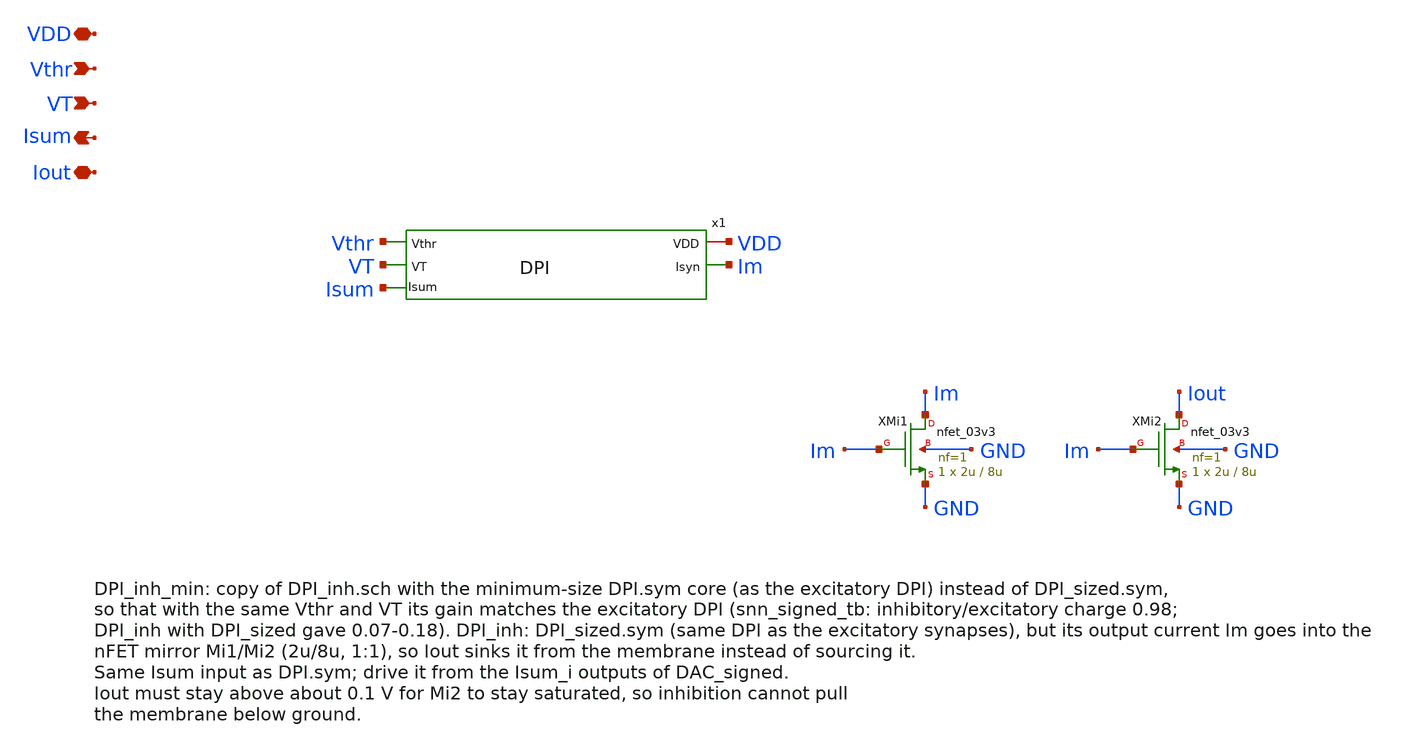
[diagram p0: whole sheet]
** sch_path: analog/DPI/DPI_inh_min.sch
**.subckt DPI_inh_min VDD Vthr VT Isum Iout
*.iopin VDD
*.ipin Vthr
*.ipin VT
*.opin Isum
*.iopin Iout
x1 VDD Vthr Im Isum VT DPI
XMi1 Im Im GND GND nfet_03v3 L=8u W=2u nf=1 ad='int((nf+1)/2) * W/nf * 0.18u' as='int((nf+2)/2) * W/nf * 0.18u'
+ pd='2*int((nf+1)/2) * (W/nf + 0.18u)' ps='2*int((nf+2)/2) * (W/nf + 0.18u)' nrd='0.18u / W' nrs='0.18u / W'
+ sa=0 sb=0 sd=0 m=1
XMi2 Iout Im GND GND nfet_03v3 L=8u W=2u nf=1 ad='int((nf+1)/2) * W/nf * 0.18u' as='int((nf+2)/2) * W/nf * 0.18u'
+ pd='2*int((nf+1)/2) * (W/nf + 0.18u)' ps='2*int((nf+2)/2) * (W/nf + 0.18u)' nrd='0.18u / W' nrs='0.18u / W'
+ sa=0 sb=0 sd=0 m=1
**.ends

* expanding   symbol:  DPI.sym # of pins=5
** sym_path: analog/neuron/DPI.sym
** sch_path: analog/neuron/DPI.sch
.subckt DPI VDD Vthr Isyn Isum VT
*.ipin Vthr
*.iopin VDD
*.opin Isyn
*.opin Isum
*.ipin VT
XM1 VDD Vthr Isum Isum nfet_03v3 L=0.28u W=0.22u nf=1 ad='int((nf+1)/2) * W/nf * 0.18u' as='int((nf+2)/2) * W/nf * 0.18u'
+ pd='2*int((nf+1)/2) * (W/nf + 0.18u)' ps='2*int((nf+2)/2) * (W/nf + 0.18u)' nrd='0.18u / W' nrs='0.18u / W'
+ sa=0 sb=0 sd=0 m=1
XM2 net1 net1 Isum Isum nfet_03v3 L=0.28u W=0.22u nf=1 ad='int((nf+1)/2) * W/nf * 0.18u' as='int((nf+2)/2) * W/nf * 0.18u'
+ pd='2*int((nf+1)/2) * (W/nf + 0.18u)' ps='2*int((nf+2)/2) * (W/nf + 0.18u)' nrd='0.18u / W' nrs='0.18u / W'
+ sa=0 sb=0 sd=0 m=1
XM3 net1 VT VDD VDD pfet_03v3 L=0.28u W=0.22u nf=1 ad='int((nf+1)/2) * W/nf * 0.18u' as='int((nf+2)/2) * W/nf * 0.18u'
+ pd='2*int((nf+1)/2) * (W/nf + 0.18u)' ps='2*int((nf+2)/2) * (W/nf + 0.18u)' nrd='0.18u / W' nrs='0.18u / W'
+ sa=0 sb=0 sd=0 m=1
XM4 Isyn net1 VDD VDD pfet_03v3 L=0.28u W=0.22u nf=1 ad='int((nf+1)/2) * W/nf * 0.18u' as='int((nf+2)/2) * W/nf * 0.18u'
+ pd='2*int((nf+1)/2) * (W/nf + 0.18u)' ps='2*int((nf+2)/2) * (W/nf + 0.18u)' nrd='0.18u / W' nrs='0.18u / W'
+ sa=0 sb=0 sd=0 m=1
C4 VDD net1 1p m=1
.ends

.end
